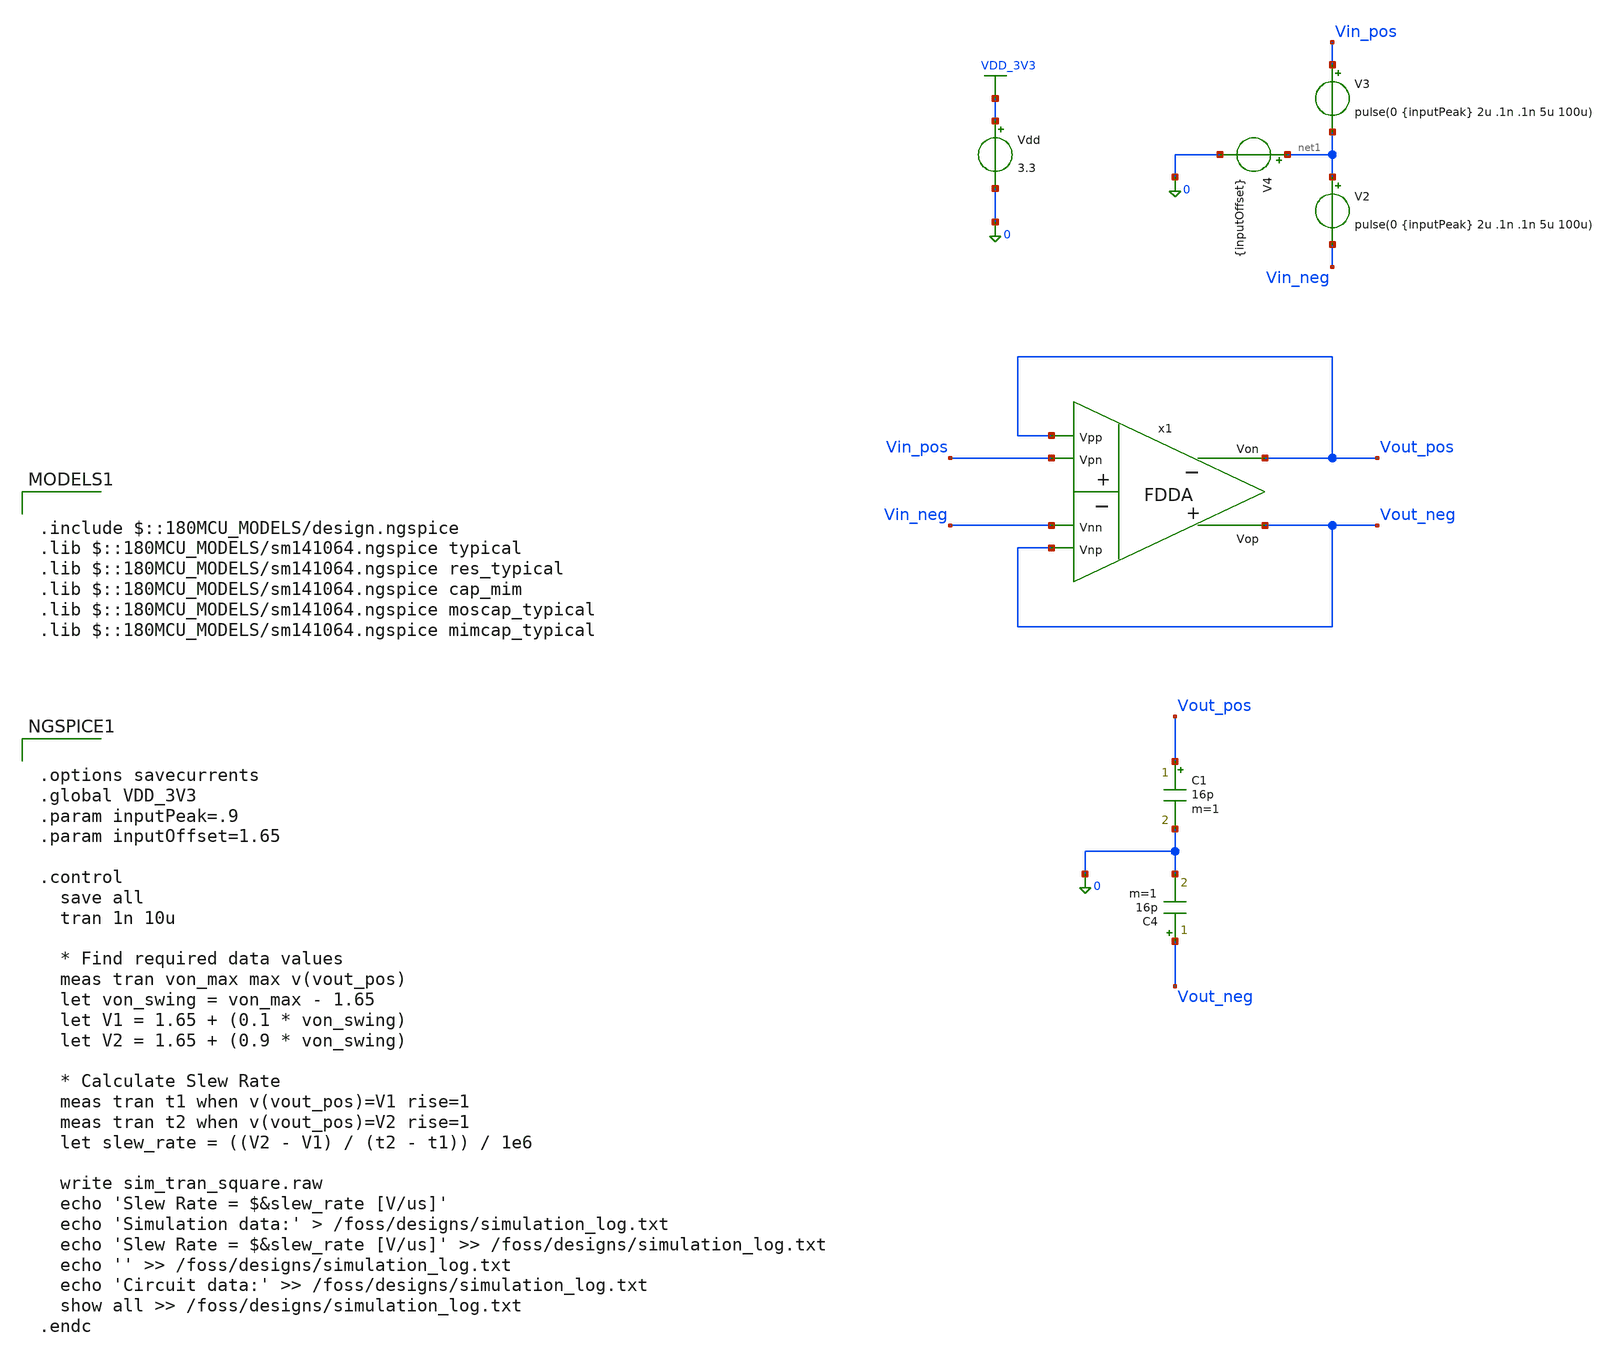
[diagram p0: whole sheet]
** sch_path: src/sim/sim_tran_square.sch
**.subckt sim_tran_square
Vdd VDD_3V3 0 3.3
.save i(vdd)
C1 Vout_pos 0 16p m=1
C4 Vout_neg 0 16p m=1
x1 Vout_pos Vout_neg Vout_neg Vin_neg Vout_pos Vin_pos fdda_subckt
V3 Vin_pos net1 pulse(0 {inputPeak} 2u .1n .1n 5u 100u)
.save i(v3)
V2 net1 Vin_neg pulse(0 {inputPeak} 2u .1n .1n 5u 100u)
.save i(v2)
V4 net1 0 {inputOffset}
.save i(v4)
**** begin user architecture code

.include $::180MCU_MODELS/design.ngspice
.lib $::180MCU_MODELS/sm141064.ngspice typical
.lib $::180MCU_MODELS/sm141064.ngspice res_typical
.lib $::180MCU_MODELS/sm141064.ngspice cap_mim
.lib $::180MCU_MODELS/sm141064.ngspice moscap_typical
.lib $::180MCU_MODELS/sm141064.ngspice mimcap_typical




.options savecurrents
.global VDD_3V3
.param inputPeak=.9
.param inputOffset=1.65

.control
  save all
  tran 1n 10u

  * Find required data values
  meas tran von_max max v(vout_pos)
  let von_swing = von_max - 1.65
  let V1 = 1.65 + (0.1 * von_swing)
  let V2 = 1.65 + (0.9 * von_swing)

  * Calculate Slew Rate
  meas tran t1 when v(vout_pos)=V1 rise=1
  meas tran t2 when v(vout_pos)=V2 rise=1
  let slew_rate = ((V2 - V1) / (t2 - t1)) / 1e6

  write sim_tran_square.raw
  echo 'Slew Rate = $&slew_rate [V/us]'
  echo 'Simulation data:' > /foss/designs/simulation_log.txt
  echo 'Slew Rate = $&slew_rate [V/us]' >> /foss/designs/simulation_log.txt
  echo '' >> /foss/designs/simulation_log.txt
  echo 'Circuit data:' >> /foss/designs/simulation_log.txt
  show all >> /foss/designs/simulation_log.txt
.endc


**** end user architecture code
**.ends
.GLOBAL VDD_3V3
.end
